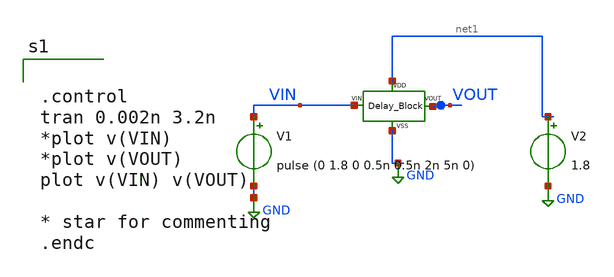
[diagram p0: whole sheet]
** sch_path: xschem/xschem_BGR_Top/Sigma_Delta/Delay_Block/Delay_Block_TB.sch
**.subckt Delay_Block_TB
V1 VIN GND pulse (0 1.8 0 0.5n 0.5n 2n 5n 0)
V2 net1 GND 1.8
X1 GND net1 VIN VOUT Delay_Block
**** begin user architecture code


.control
tran 0.002n 3.2n
*plot v(VIN)
*plot v(VOUT)
plot v(VIN) v(VOUT)

* star for commenting
.endc


** opencircuitdesign pdks install
.lib $::SKYWATER_MODELS/sky130.lib.spice tt


**** end user architecture code
**.ends

* expanding   symbol:  Sigma_Delta/Delay_Block/Delay_Block.sym # of pins=4
** sym_path: xschem/xschem_BGR_Top/Sigma_Delta/Delay_Block/Delay_Block.sym
** sch_path: xschem/xschem_BGR_Top/Sigma_Delta/Delay_Block/Delay_Block.sch
.subckt Delay_Block VSS VDD VIN VOUT
*.iopin VOUT
*.iopin VIN
*.iopin VDD
*.iopin VSS
X1 VSS VDD VIN net2 Inverter_01
X8 VSS VDD net1 VOUT Inverter_03
X2 VSS VDD net2 net3 Inverter_03
X3 VSS VDD net3 net1 Inverter_03
.ends


* expanding   symbol:  Sigma_Delta/Inverter_01/Inverter_01.sym # of pins=4
** sym_path: xschem/xschem_BGR_Top/Sigma_Delta/Inverter_01/Inverter_01.sym
** sch_path: xschem/xschem_BGR_Top/Sigma_Delta/Inverter_01/Inverter_01.sch
.subckt Inverter_01 VSS VDD VIN VOUT
*.iopin VIN
*.iopin VDD
*.iopin VSS
*.iopin VOUT
XM1 VOUT VIN VSS VSS sky130_fd_pr__nfet_01v8 L=0.48 W=0.4 nf=1 ad='int((nf+1)/2) * W/nf * 0.29' as='int((nf+2)/2) * W/nf * 0.29'
+ pd='2*int((nf+1)/2) * (W/nf + 0.29)' ps='2*int((nf+2)/2) * (W/nf + 0.29)' nrd='0.29 / W' nrs='0.29 / W'
+ sa=0 sb=0 sd=0 mult=1 m=1
XM2 VOUT VIN VDD VDD sky130_fd_pr__pfet_01v8 L=0.48 W=0.8 nf=1 ad='int((nf+1)/2) * W/nf * 0.29' as='int((nf+2)/2) * W/nf * 0.29'
+ pd='2*int((nf+1)/2) * (W/nf + 0.29)' ps='2*int((nf+2)/2) * (W/nf + 0.29)' nrd='0.29 / W' nrs='0.29 / W'
+ sa=0 sb=0 sd=0 mult=1 m=1
.ends


* expanding   symbol:  Sigma_Delta/Inverter_03/Inverter_03.sym # of pins=4
** sym_path: xschem/xschem_BGR_Top/Sigma_Delta/Inverter_03/Inverter_03.sym
** sch_path: xschem/xschem_BGR_Top/Sigma_Delta/Inverter_03/Inverter_03.sch
.subckt Inverter_03 VSS VDD VIN VOUT
*.iopin VIN
*.iopin VDD
*.iopin VSS
*.iopin VOUT
XM1 VOUT VIN VSS VSS sky130_fd_pr__nfet_01v8 L=0.25 W=0.5 nf=1 ad='int((nf+1)/2) * W/nf * 0.29' as='int((nf+2)/2) * W/nf * 0.29'
+ pd='2*int((nf+1)/2) * (W/nf + 0.29)' ps='2*int((nf+2)/2) * (W/nf + 0.29)' nrd='0.29 / W' nrs='0.29 / W'
+ sa=0 sb=0 sd=0 mult=1 m=1
XM2 VOUT VIN VDD VDD sky130_fd_pr__pfet_01v8 L=0.25 W=1 nf=1 ad='int((nf+1)/2) * W/nf * 0.29' as='int((nf+2)/2) * W/nf * 0.29'
+ pd='2*int((nf+1)/2) * (W/nf + 0.29)' ps='2*int((nf+2)/2) * (W/nf + 0.29)' nrd='0.29 / W' nrs='0.29 / W'
+ sa=0 sb=0 sd=0 mult=1 m=1
.ends

.GLOBAL GND
.end
